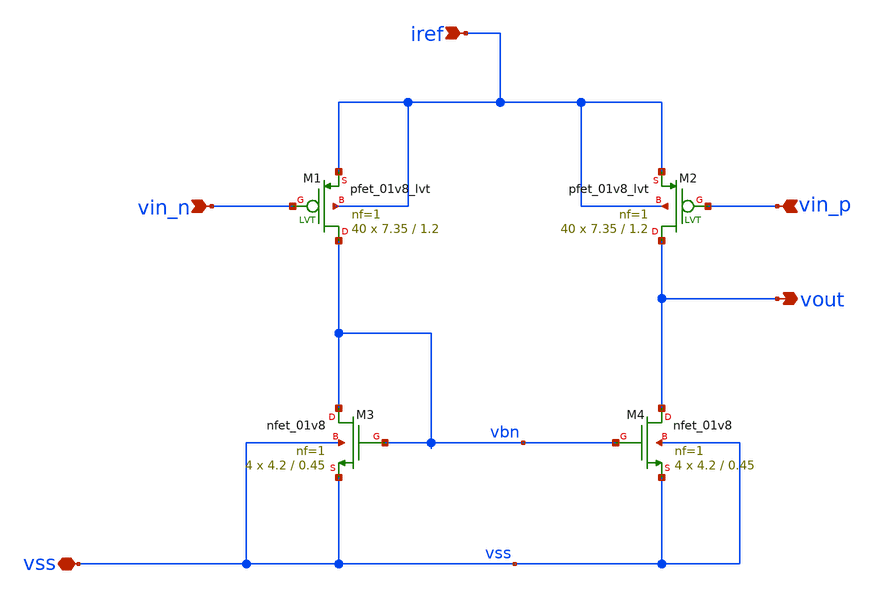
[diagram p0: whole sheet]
** sch_path: track_analogico/opamp_ramiro/input.sch
**.subckt input vss vin_n vin_p vout iref
*.iopin vss
*.ipin vin_n
*.ipin vin_p
*.opin vout
*.ipin iref
XM3 vbn vbn vss vss sky130_fd_pr__nfet_01v8 L=0.45 W=4.2 nf=1 ad='W * 0.29' as='W * 0.29' pd='2 * (W + 0.29)'
+ ps='2 * (W + 0.29)' nrd='0.29 / W' nrs='0.29 / W' sa=0 sb=0 sd=0 mult=4 m=4
XM4 vout vbn vss vss sky130_fd_pr__nfet_01v8 L=0.45 W=4.2 nf=1 ad='W * 0.29' as='W * 0.29' pd='2 * (W + 0.29)'
+ ps='2 * (W + 0.29)' nrd='0.29 / W' nrs='0.29 / W' sa=0 sb=0 sd=0 mult=4 m=4
XM1 vbn vin_n iref iref sky130_fd_pr__pfet_01v8_lvt L=1.2 W=7.35 nf=1 ad='int((nf+1)/2) * W/nf * 0.29'
+ as='int((nf+2)/2) * W/nf * 0.29' pd='2*int((nf+1)/2) * (W/nf + 0.29)' ps='2*int((nf+2)/2) * (W/nf + 0.29)'
+ nrd='0.29 / W' nrs='0.29 / W' sa=0 sb=0 sd=0 mult=40 m=40
XM2 vout vin_p iref iref sky130_fd_pr__pfet_01v8_lvt L=1.2 W=7.35 nf=1 ad='int((nf+1)/2) * W/nf * 0.29'
+ as='int((nf+2)/2) * W/nf * 0.29' pd='2*int((nf+1)/2) * (W/nf + 0.29)' ps='2*int((nf+2)/2) * (W/nf + 0.29)'
+ nrd='0.29 / W' nrs='0.29 / W' sa=0 sb=0 sd=0 mult=40 m=40
**.ends
.end
